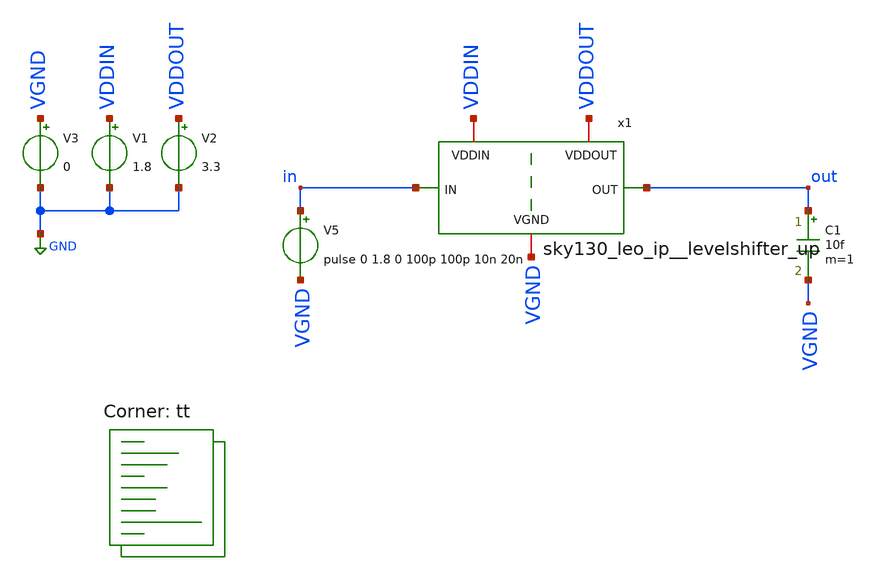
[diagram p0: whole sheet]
** sch_path: tt_um_tt08_aicd_playground/dependencies/sky130_leo_ip__levelshifter/xschem/sky130_leo_ip__levelshifter_up_tb.sch
**.subckt sky130_leo_ip__levelshifter_up_tb
x1 VDDOUT VDDIN out in VGND sky130_leo_ip__levelshifter_up
V1 VDDIN GND 1.8
V2 VDDOUT GND 3.3
V3 VGND GND 0
C1 out VGND 10f m=1
V5 in VGND pulse 0 1.8 0 100p 100p 10n 20n
**** begin user architecture code
.lib $::SKYWATER_MODELS/sky130.lib.spice tt



.param vddin = 1.8
.param vddout = 3.3

*.include {DUT_path}

.control
    save all

    *** ADD SAVE LINES HERE -- TEMPLATE for NMOS M1 and PMOS M2 given below, copy and adjust device
+ name
    *save @m.x1.xm1.msky130_fd_pr__nfet_01v8_lvt[id] @m.x1.xm1.msky130_fd_pr__nfet_01v8_lvt[gm]
+ @m.x1.xm1.msky130_fd_pr__nfet_01v8_lvt[gds]
    *save @m.x1.xm2.msky130_fd_pr__pfet_01v8_lvt[id] @m.x1.xm2.msky130_fd_pr__pfet_01v8_lvt[gm]
+ @m.x1.xm2.msky130_fd_pr__pfet_01v8_lvt[gds]

    * operating point
    op
    write tb.raw
    set appendwrite

    * transient simulation
    options method=gear
    tran 1p 40n
    save all
    write tb.raw

    * measure parameters

    * get the peak-to-peak voltage
    meas TRAN range PP v(out)
    let ten=0.1*range
    let ninety=0.9*range

    print range ten ninety

    # rise and fall time
    meas TRAN rise_time TRIG v(out) VAL=ten    TD=0ns  RISE=1   TARG v(out) VAL=ninety TD=0ns
+  RISE=1
    meas TRAN fall_time TRIG v(out) VAL=ninety TD=5ns  FALL=1   TARG v(out) VAL=TEN    TD=5ns
+  FALL=1

    print rise_time fall_time

    *echo $&ugf > {simpath}/{filename}_{N}.data

.endc



**** end user architecture code
**.ends

* expanding   symbol:  sky130_leo_ip__levelshifter_up.sym # of pins=5
** sym_path: tt_um_tt08_aicd_playground/dependencies/sky130_leo_ip__levelshifter/xschem/sky130_leo_ip__levelshifter_up.sym
** sch_path: tt_um_tt08_aicd_playground/dependencies/sky130_leo_ip__levelshifter/xschem/sky130_leo_ip__levelshifter_up.sch
.subckt sky130_leo_ip__levelshifter_up VDDOUT VDDIN OUT IN VGND
*.ipin IN
*.iopin VGND
*.iopin VDDIN
*.opin OUT
*.iopin VDDOUT
XM1 ctrl_n IN VGND VGND sky130_fd_pr__nfet_01v8 L=0.15 W=0.42 nf=1 ad='int((nf+1)/2) * W/nf * 0.29' as='int((nf+2)/2) * W/nf * 0.29'
+ pd='2*int((nf+1)/2) * (W/nf + 0.29)' ps='2*int((nf+2)/2) * (W/nf + 0.29)' nrd='0.29 / W' nrs='0.29 / W'
+ sa=0 sb=0 sd=0 mult=1 m=1
XM2 ctrl_n IN VDDIN VDDIN sky130_fd_pr__pfet_01v8 L=0.15 W=1 nf=1 ad='int((nf+1)/2) * W/nf * 0.29' as='int((nf+2)/2) * W/nf * 0.29'
+ pd='2*int((nf+1)/2) * (W/nf + 0.29)' ps='2*int((nf+2)/2) * (W/nf + 0.29)' nrd='0.29 / W' nrs='0.29 / W'
+ sa=0 sb=0 sd=0 mult=1 m=1
XM3 ctrl ctrl_n VGND VGND sky130_fd_pr__nfet_01v8 L=0.15 W=0.42 nf=1 ad='int((nf+1)/2) * W/nf * 0.29'
+ as='int((nf+2)/2) * W/nf * 0.29' pd='2*int((nf+1)/2) * (W/nf + 0.29)' ps='2*int((nf+2)/2) * (W/nf + 0.29)'
+ nrd='0.29 / W' nrs='0.29 / W' sa=0 sb=0 sd=0 mult=1 m=1
XM4 ctrl ctrl_n VDDIN VDDIN sky130_fd_pr__pfet_01v8 L=0.15 W=1 nf=1 ad='int((nf+1)/2) * W/nf * 0.29'
+ as='int((nf+2)/2) * W/nf * 0.29' pd='2*int((nf+1)/2) * (W/nf + 0.29)' ps='2*int((nf+2)/2) * (W/nf + 0.29)'
+ nrd='0.29 / W' nrs='0.29 / W' sa=0 sb=0 sd=0 mult=1 m=1
XM5 OUT p1 VDDOUT VDDOUT sky130_fd_pr__pfet_g5v0d10v5 L=0.5 W=0.42 nf=1 ad='int((nf+1)/2) * W/nf * 0.29'
+ as='int((nf+2)/2) * W/nf * 0.29' pd='2*int((nf+1)/2) * (W/nf + 0.29)' ps='2*int((nf+2)/2) * (W/nf + 0.29)'
+ nrd='0.29 / W' nrs='0.29 / W' sa=0 sb=0 sd=0 mult=1 m=1
XM6 p1 ctrl VGND VGND sky130_fd_pr__nfet_g5v0d10v5 L=0.5 W=1 nf=1 ad='int((nf+1)/2) * W/nf * 0.29' as='int((nf+2)/2) * W/nf * 0.29'
+ pd='2*int((nf+1)/2) * (W/nf + 0.29)' ps='2*int((nf+2)/2) * (W/nf + 0.29)' nrd='0.29 / W' nrs='0.29 / W'
+ sa=0 sb=0 sd=0 mult=1 m=1
XM7 p1 OUT VDDOUT VDDOUT sky130_fd_pr__pfet_g5v0d10v5 L=0.5 W=0.42 nf=1 ad='int((nf+1)/2) * W/nf * 0.29'
+ as='int((nf+2)/2) * W/nf * 0.29' pd='2*int((nf+1)/2) * (W/nf + 0.29)' ps='2*int((nf+2)/2) * (W/nf + 0.29)'
+ nrd='0.29 / W' nrs='0.29 / W' sa=0 sb=0 sd=0 mult=1 m=1
XM8 OUT ctrl_n VGND VGND sky130_fd_pr__nfet_g5v0d10v5 L=0.5 W=1 nf=1 ad='int((nf+1)/2) * W/nf * 0.29'
+ as='int((nf+2)/2) * W/nf * 0.29' pd='2*int((nf+1)/2) * (W/nf + 0.29)' ps='2*int((nf+2)/2) * (W/nf + 0.29)'
+ nrd='0.29 / W' nrs='0.29 / W' sa=0 sb=0 sd=0 mult=1 m=1
.ends

.GLOBAL GND
.end
